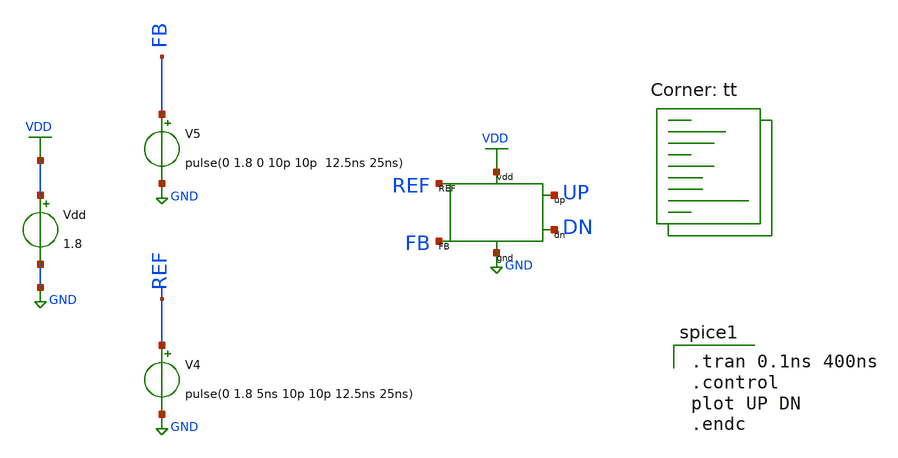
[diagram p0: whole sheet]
** sch_path: pll/pfd_cp_lf_lib/PFD_tb/xschem/PFD_tb.sch
**.subckt PFD_tb
X1 REF UP FB VDD GND DN PFD
Vdd VDD GND 1.8
V4 REF GND pulse(0 1.8 5ns 10p 10p 12.5ns 25ns)
V5 FB GND pulse(0 1.8 0 10p 10p 12.5ns 25ns)
**** begin user architecture code
.lib $::SKYWATER_MODELS/sky130.lib.spice tt

.tran 0.1ns 400ns
.control
plot UP DN
.endc


** opencircuitdesign pdks install
.lib $::SKYWATER_MODELS/sky130.lib.spice tt


**** end user architecture code
**.ends

* expanding   symbol:  ../../PFD/xschem/PFD.sym # of pins=6
** sym_path: pll/pfd_cp_lf_lib/PFD/xschem/PFD.sym
** sch_path: pll/pfd_cp_lf_lib/PFD/xschem/PFD.sch
.subckt PFD REF up FB VDD GND dn
*.iopin VDD
*.iopin GND
*.ipin REF
*.ipin FB
*.opin up
*.opin dn
XM3 net3 FB net1 GND sky130_fd_pr__nfet_01v8 L=0.15 W=2.5 nf=2 ad='int((nf+1)/2) * W/nf * 0.29' as='int((nf+2)/2) * W/nf * 0.29'
+ pd='2*int((nf+1)/2) * (W/nf + 0.29)' ps='2*int((nf+2)/2) * (W/nf + 0.29)' nrd='0.29 / W' nrs='0.29 / W'
+ sa=0 sb=0 sd=0 mult=1 m=1
XM4 net4 REF net2 GND sky130_fd_pr__nfet_01v8 L=0.15 W=2.5 nf=2 ad='int((nf+1)/2) * W/nf * 0.29' as='int((nf+2)/2) * W/nf * 0.29'
+ pd='2*int((nf+1)/2) * (W/nf + 0.29)' ps='2*int((nf+2)/2) * (W/nf + 0.29)' nrd='0.29 / W' nrs='0.29 / W'
+ sa=0 sb=0 sd=0 mult=1 m=1
XM5 dn REF GND GND sky130_fd_pr__nfet_01v8 L=0.15 W=1 nf=2 ad='int((nf+1)/2) * W/nf * 0.29' as='int((nf+2)/2) * W/nf * 0.29'
+ pd='2*int((nf+1)/2) * (W/nf + 0.29)' ps='2*int((nf+2)/2) * (W/nf + 0.29)' nrd='0.29 / W' nrs='0.29 / W'
+ sa=0 sb=0 sd=0 mult=1 m=1
XM6 dn net3 GND GND sky130_fd_pr__nfet_01v8 L=0.15 W=1 nf=2 ad='int((nf+1)/2) * W/nf * 0.29' as='int((nf+2)/2) * W/nf * 0.29'
+ pd='2*int((nf+1)/2) * (W/nf + 0.29)' ps='2*int((nf+2)/2) * (W/nf + 0.29)' nrd='0.29 / W' nrs='0.29 / W'
+ sa=0 sb=0 sd=0 mult=1 m=1
XM7 up net4 GND GND sky130_fd_pr__nfet_01v8 L=0.15 W=1 nf=2 ad='int((nf+1)/2) * W/nf * 0.29' as='int((nf+2)/2) * W/nf * 0.29'
+ pd='2*int((nf+1)/2) * (W/nf + 0.29)' ps='2*int((nf+2)/2) * (W/nf + 0.29)' nrd='0.29 / W' nrs='0.29 / W'
+ sa=0 sb=0 sd=0 mult=1 m=1
XM8 up FB GND GND sky130_fd_pr__nfet_01v8 L=0.15 W=1 nf=2 ad='int((nf+1)/2) * W/nf * 0.29' as='int((nf+2)/2) * W/nf * 0.29'
+ pd='2*int((nf+1)/2) * (W/nf + 0.29)' ps='2*int((nf+2)/2) * (W/nf + 0.29)' nrd='0.29 / W' nrs='0.29 / W'
+ sa=0 sb=0 sd=0 mult=1 m=1
XM9 net4 REF net5 VDD sky130_fd_pr__pfet_01v8 L=0.15 W=2.5 nf=1 ad='int((nf+1)/2) * W/nf * 0.29' as='int((nf+2)/2) * W/nf * 0.29'
+ pd='2*int((nf+1)/2) * (W/nf + 0.29)' ps='2*int((nf+2)/2) * (W/nf + 0.29)' nrd='0.29 / W' nrs='0.29 / W'
+ sa=0 sb=0 sd=0 mult=1 m=1
XM1 net5 FB VDD VDD sky130_fd_pr__pfet_01v8 L=0.15 W=2.5 nf=1 ad='int((nf+1)/2) * W/nf * 0.29' as='int((nf+2)/2) * W/nf * 0.29'
+ pd='2*int((nf+1)/2) * (W/nf + 0.29)' ps='2*int((nf+2)/2) * (W/nf + 0.29)' nrd='0.29 / W' nrs='0.29 / W'
+ sa=0 sb=0 sd=0 mult=1 m=1
XM2 net3 FB net6 VDD sky130_fd_pr__pfet_01v8 L=0.15 W=2.5 nf=1 ad='int((nf+1)/2) * W/nf * 0.29' as='int((nf+2)/2) * W/nf * 0.29'
+ pd='2*int((nf+1)/2) * (W/nf + 0.29)' ps='2*int((nf+2)/2) * (W/nf + 0.29)' nrd='0.29 / W' nrs='0.29 / W'
+ sa=0 sb=0 sd=0 mult=1 m=1
XM10 net6 REF VDD VDD sky130_fd_pr__pfet_01v8 L=0.15 W=2.5 nf=1 ad='int((nf+1)/2) * W/nf * 0.29' as='int((nf+2)/2) * W/nf * 0.29'
+ pd='2*int((nf+1)/2) * (W/nf + 0.29)' ps='2*int((nf+2)/2) * (W/nf + 0.29)' nrd='0.29 / W' nrs='0.29 / W'
+ sa=0 sb=0 sd=0 mult=1 m=1
XM13 dn net3 net7 VDD sky130_fd_pr__pfet_01v8 L=0.15 W=2 nf=2 ad='int((nf+1)/2) * W/nf * 0.29' as='int((nf+2)/2) * W/nf * 0.29'
+ pd='2*int((nf+1)/2) * (W/nf + 0.29)' ps='2*int((nf+2)/2) * (W/nf + 0.29)' nrd='0.29 / W' nrs='0.29 / W'
+ sa=0 sb=0 sd=0 mult=1 m=1
XM14 net7 REF VDD VDD sky130_fd_pr__pfet_01v8 L=0.15 W=2 nf=2 ad='int((nf+1)/2) * W/nf * 0.29' as='int((nf+2)/2) * W/nf * 0.29'
+ pd='2*int((nf+1)/2) * (W/nf + 0.29)' ps='2*int((nf+2)/2) * (W/nf + 0.29)' nrd='0.29 / W' nrs='0.29 / W'
+ sa=0 sb=0 sd=0 mult=1 m=1
XM15 up net4 net8 VDD sky130_fd_pr__pfet_01v8 L=0.15 W=2 nf=2 ad='int((nf+1)/2) * W/nf * 0.29' as='int((nf+2)/2) * W/nf * 0.29'
+ pd='2*int((nf+1)/2) * (W/nf + 0.29)' ps='2*int((nf+2)/2) * (W/nf + 0.29)' nrd='0.29 / W' nrs='0.29 / W'
+ sa=0 sb=0 sd=0 mult=1 m=1
XM16 net8 FB VDD VDD sky130_fd_pr__pfet_01v8 L=0.15 W=2 nf=2 ad='int((nf+1)/2) * W/nf * 0.29' as='int((nf+2)/2) * W/nf * 0.29'
+ pd='2*int((nf+1)/2) * (W/nf + 0.29)' ps='2*int((nf+2)/2) * (W/nf + 0.29)' nrd='0.29 / W' nrs='0.29 / W'
+ sa=0 sb=0 sd=0 mult=1 m=1
XM11 net1 net4 GND GND sky130_fd_pr__nfet_01v8 L=0.15 W=2.5 nf=2 ad='int((nf+1)/2) * W/nf * 0.29' as='int((nf+2)/2) * W/nf * 0.29'
+ pd='2*int((nf+1)/2) * (W/nf + 0.29)' ps='2*int((nf+2)/2) * (W/nf + 0.29)' nrd='0.29 / W' nrs='0.29 / W'
+ sa=0 sb=0 sd=0 mult=1 m=1
XM12 net2 net3 GND GND sky130_fd_pr__nfet_01v8 L=0.15 W=2.5 nf=2 ad='int((nf+1)/2) * W/nf * 0.29' as='int((nf+2)/2) * W/nf * 0.29'
+ pd='2*int((nf+1)/2) * (W/nf + 0.29)' ps='2*int((nf+2)/2) * (W/nf + 0.29)' nrd='0.29 / W' nrs='0.29 / W'
+ sa=0 sb=0 sd=0 mult=1 m=1
.ends

.GLOBAL GND
.GLOBAL VDD
.end
